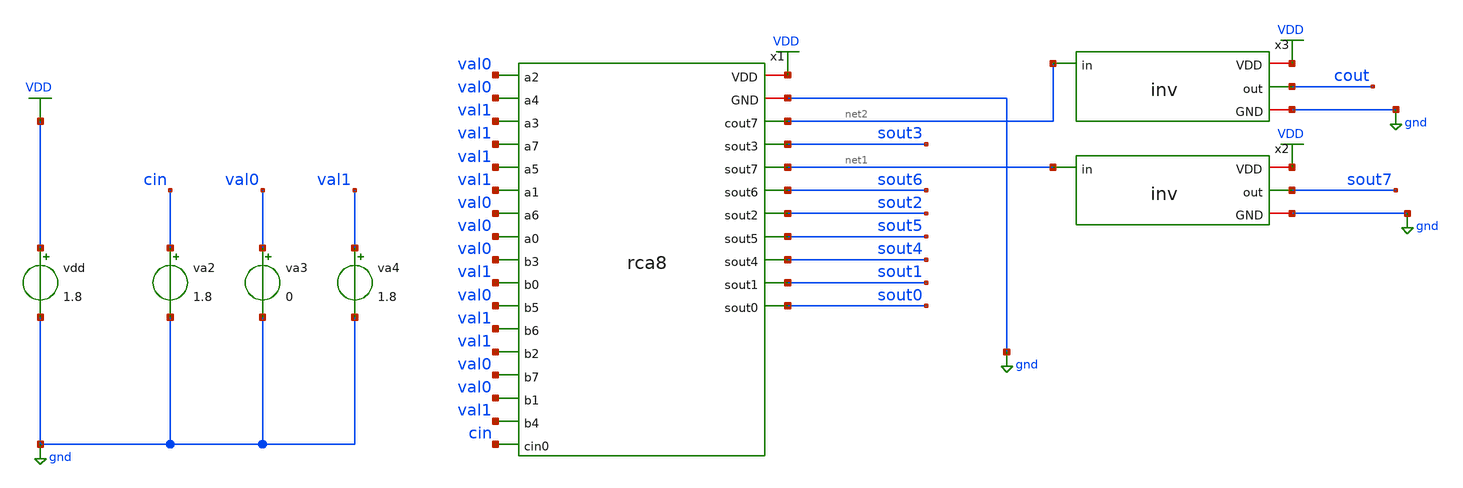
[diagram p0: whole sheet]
** sch_path: assignments/assignment8/assignrca1.sch
**.subckt assignrca1
x1 net2 cin val1 val0 val0 val1 val1 val0 val0 val1 val1 val0 val0 val1 val1 val0 val0 val1 sout0
+ sout1 sout2 sout3 sout4 sout5 sout6 net1 gnd VDD rca8
vdd VDD gnd 1.8
va3 val0 gnd 0
va4 val1 gnd 1.8
va2 cin gnd 1.8
x2 VDD net1 sout7 gnd inv
x3 VDD net2 cout gnd inv
**** begin user architecture code


.include rca8_extracted.spice
.save all
.control
alter @va2[pulse] = [ 0 1.8 0 10p 10p 4n 8n ]
tran 5p 40n

* cin -> cout7 (adder output, before the load inverter x3)
meas tran c_delay_fall TRIG v(cin) VAL=0.9 RISE=3 TARG v(cout) VAL=0.9 FALL=3
meas tran c_delay_rise TRIG v(cin) VAL=0.9 FALL=3 TARG v(cout) VAL=0.9 RISE=3

* cin -> sum7 (adder output, before the output inverter x2)
meas tran s_delay_rise TRIG v(cin) VAL=0.9 RISE=3 TARG v(sout7) VAL=0.9 RISE=3
meas tran s_delay_fall TRIG v(cin) VAL=0.9 FALL=3 TARG v(sout7) VAL=0.9 FALL=3

let cin_to_cout=(c_delay_rise+c_delay_fall)/2
let cin_to_s7=(s_delay_rise+s_delay_fall)/2
print cin_to_cout cin_to_s7
plot v(cin) v(net2) v(net1)
.endc


.lib $::SKYWATER_MODELS/sky130.lib.spice tt
**** end user architecture code
**.ends

* expanding   symbol:  inv.sym # of pins=4
** sym_path: assignments/assignment6/inv.sym
** sch_path: assignments/assignment6/inv.sch
.subckt inv VDD in out GND
*.ipin in
*.iopin GND
*.iopin VDD
*.opin out
XM3 out in GND GND sky130_fd_pr__nfet_01v8 L=0.15 W=0.42 nf=1 ad='int((nf+1)/2) * W/nf * 0.29' as='int((nf+2)/2) * W/nf * 0.29'
+ pd='2*int((nf+1)/2) * (W/nf + 0.29)' ps='2*int((nf+2)/2) * (W/nf + 0.29)' nrd='0.29 / W' nrs='0.29 / W'
+ sa=0 sb=0 sd=0 mult=1 m=1
XM4 out in VDD VDD sky130_fd_pr__pfet_01v8 L=0.15 W=0.84 nf=1 ad='int((nf+1)/2) * W/nf * 0.29' as='int((nf+2)/2) * W/nf * 0.29'
+ pd='2*int((nf+1)/2) * (W/nf + 0.29)' ps='2*int((nf+2)/2) * (W/nf + 0.29)' nrd='0.29 / W' nrs='0.29 / W'
+ sa=0 sb=0 sd=0 mult=1 m=1
.ends

.GLOBAL VDD
.GLOBAL gnd
.end
